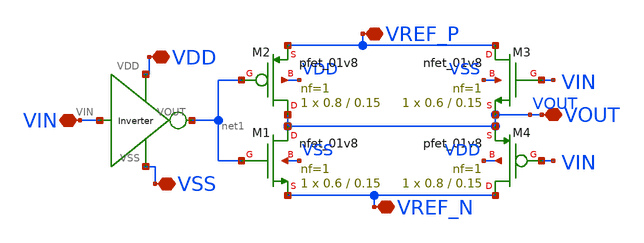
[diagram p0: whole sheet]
** sch_path: xschem/xschem_BGR_Top/Sigma_Delta/1_bit_DAC/1_bit_DAC.sch
**.subckt 1_bit_DAC VIN VDD VSS VREF_P VREF_N VOUT
*.iopin VIN
*.iopin VDD
*.iopin VSS
*.iopin VREF_P
*.iopin VREF_N
*.iopin VOUT
XM1 VOUT net1 VREF_N VSS sky130_fd_pr__nfet_01v8 L=0.15 W=0.6 nf=1 ad='int((nf+1)/2) * W/nf * 0.29' as='int((nf+2)/2) * W/nf * 0.29'
+ pd='2*int((nf+1)/2) * (W/nf + 0.29)' ps='2*int((nf+2)/2) * (W/nf + 0.29)' nrd='0.29 / W' nrs='0.29 / W'
+ sa=0 sb=0 sd=0 mult=1 m=1
XM3 VREF_P VIN VOUT VSS sky130_fd_pr__nfet_01v8 L=0.15 W=0.6 nf=1 ad='int((nf+1)/2) * W/nf * 0.29' as='int((nf+2)/2) * W/nf * 0.29'
+ pd='2*int((nf+1)/2) * (W/nf + 0.29)' ps='2*int((nf+2)/2) * (W/nf + 0.29)' nrd='0.29 / W' nrs='0.29 / W'
+ sa=0 sb=0 sd=0 mult=1 m=1
XM4 VREF_N VIN VOUT VDD sky130_fd_pr__pfet_01v8 L=0.15 W=0.8 nf=1 ad='int((nf+1)/2) * W/nf * 0.29' as='int((nf+2)/2) * W/nf * 0.29'
+ pd='2*int((nf+1)/2) * (W/nf + 0.29)' ps='2*int((nf+2)/2) * (W/nf + 0.29)' nrd='0.29 / W' nrs='0.29 / W'
+ sa=0 sb=0 sd=0 mult=1 m=1
X1 VSS VDD VIN net1 Inverter
XM2 VOUT net1 VREF_P VDD sky130_fd_pr__pfet_01v8 L=0.15 W=0.8 nf=1 ad='int((nf+1)/2) * W/nf * 0.29' as='int((nf+2)/2) * W/nf * 0.29'
+ pd='2*int((nf+1)/2) * (W/nf + 0.29)' ps='2*int((nf+2)/2) * (W/nf + 0.29)' nrd='0.29 / W' nrs='0.29 / W'
+ sa=0 sb=0 sd=0 mult=1 m=1
**** begin user architecture code

** opencircuitdesign pdks install
.lib $::SKYWATER_MODELS/sky130.lib.spice tt


**** end user architecture code
**.ends

* expanding   symbol:  Sigma_Delta/Inverter/Inverter.sym # of pins=4
** sym_path: xschem/xschem_BGR_Top/Sigma_Delta/Inverter/Inverter.sym
** sch_path: xschem/xschem_BGR_Top/Sigma_Delta/Inverter/Inverter.sch
.subckt Inverter VSS VDD VIN VOUT
*.ipin VIN
*.iopin VDD
*.iopin VSS
*.opin VOUT
XM1 VOUT VIN VSS VSS sky130_fd_pr__nfet_01v8 L=0.15 W=0.9 nf=1 ad='int((nf+1)/2) * W/nf * 0.29' as='int((nf+2)/2) * W/nf * 0.29'
+ pd='2*int((nf+1)/2) * (W/nf + 0.29)' ps='2*int((nf+2)/2) * (W/nf + 0.29)' nrd='0.29 / W' nrs='0.29 / W'
+ sa=0 sb=0 sd=0 mult=1 m=1
XM2 VOUT VIN VDD VDD sky130_fd_pr__pfet_01v8 L=0.15 W=0.9 nf=2 ad='int((nf+1)/2) * W/nf * 0.29' as='int((nf+2)/2) * W/nf * 0.29'
+ pd='2*int((nf+1)/2) * (W/nf + 0.29)' ps='2*int((nf+2)/2) * (W/nf + 0.29)' nrd='0.29 / W' nrs='0.29 / W'
+ sa=0 sb=0 sd=0 mult=1 m=1
.ends

.end
